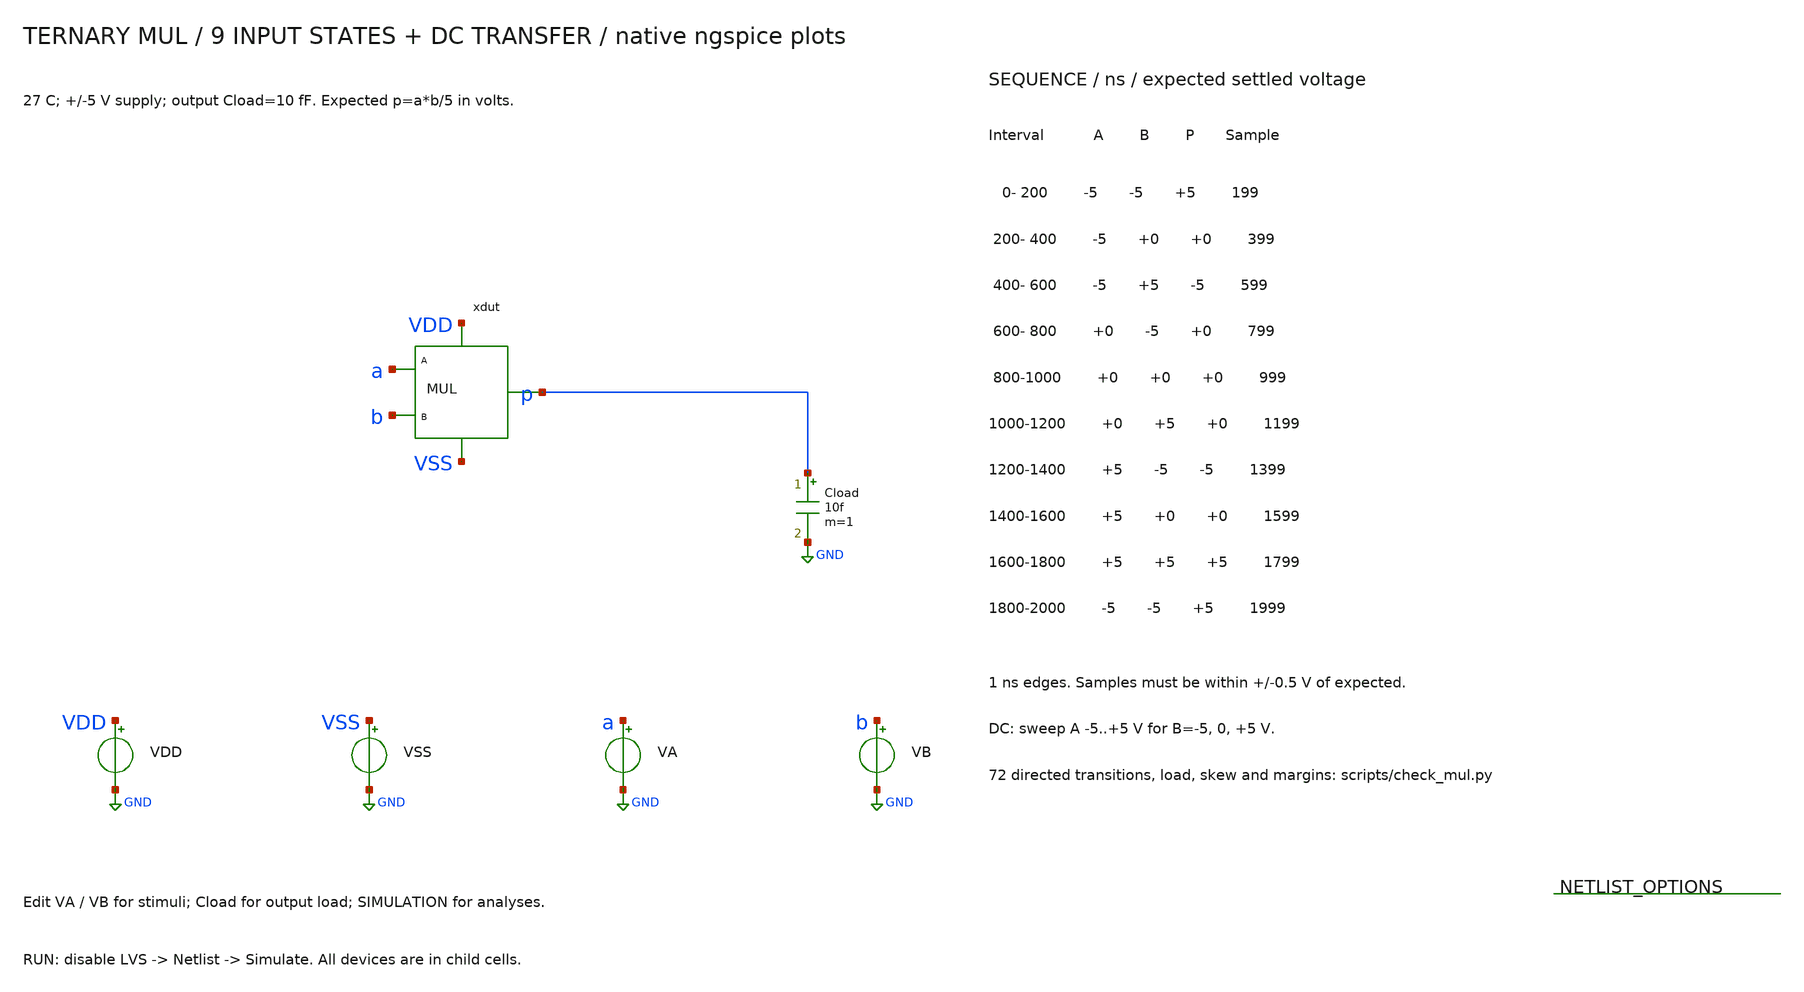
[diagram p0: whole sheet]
** sch_path: mul_tb.sch
**.subckt mul_tb
xdut a b p VDD VSS mul
Cload p GND 10f m=1
VDD VDD GND 5
VSS VSS GND -5
VA a GND PWL(0 -5 200n -5 201n -5 400n -5 401n -5 600n -5 601n 0 800n 0 801n 0 1000n 0 1001n 0 1200n
+ 0 1201n 5 1400n 5 1401n 5 1600n 5 1601n 5 1800n 5 1801n -5 2000n -5)
VB b GND PWL(0 -5 200n -5 201n 0 400n 0 401n 5 600n 5 601n -5 800n -5 801n 0 1000n 0 1001n 5 1200n 5
+ 1201n -5 1400n -5 1401n 0 1600n 0 1601n 5 1800n 5 1801n -5 2000n -5)
**** begin user architecture code
 .include $::LIB/ip62_models

.temp 27
.options rshunt=1e12
.nodeset v(p)=5 v(xdut.t1)=5 v(xdut.t2)=5 v(xdut.t3)=-5
.control
save all
set wr_singlescale
set wr_vecnames
setplot const
let failures=0
alter VB dc=-5
dc VA -5 5 0.03125
meas dc dc_0_0 find v(p) at=-5
if abs(dc_0_0-(5.0)) > 0.5
let const.failures=const.failures+1
echo FAIL: dc_0_0 expected 5.0 V
end
meas dc dc_0_1 find v(p) at=0
if abs(dc_0_1-(0.0)) > 0.5
let const.failures=const.failures+1
echo FAIL: dc_0_1 expected 0.0 V
end
meas dc dc_0_2 find v(p) at=5
if abs(dc_0_2-(-5.0)) > 0.5
let const.failures=const.failures+1
echo FAIL: dc_0_2 expected -5.0 V
end
plot v(a) v(p) ylimit -5.5 5.5 title 'MUL DC: B=-5 V'
wrdata mul_dc_0.txt v(a) v(p) v(xdut.t1) v(xdut.t2) v(xdut.t3)
alter VB dc=0
dc VA -5 5 0.03125
meas dc dc_1_0 find v(p) at=-5
if abs(dc_1_0-(0.0)) > 0.5
let const.failures=const.failures+1
echo FAIL: dc_1_0 expected 0.0 V
end
meas dc dc_1_1 find v(p) at=0
if abs(dc_1_1-(0.0)) > 0.5
let const.failures=const.failures+1
echo FAIL: dc_1_1 expected 0.0 V
end
meas dc dc_1_2 find v(p) at=5
if abs(dc_1_2-(0.0)) > 0.5
let const.failures=const.failures+1
echo FAIL: dc_1_2 expected 0.0 V
end
plot v(a) v(p) ylimit -5.5 5.5 title 'MUL DC: B=0 V'
wrdata mul_dc_1.txt v(a) v(p) v(xdut.t1) v(xdut.t2) v(xdut.t3)
alter VB dc=5
dc VA -5 5 0.03125
meas dc dc_2_0 find v(p) at=-5
if abs(dc_2_0-(-5.0)) > 0.5
let const.failures=const.failures+1
echo FAIL: dc_2_0 expected -5.0 V
end
meas dc dc_2_1 find v(p) at=0
if abs(dc_2_1-(0.0)) > 0.5
let const.failures=const.failures+1
echo FAIL: dc_2_1 expected 0.0 V
end
meas dc dc_2_2 find v(p) at=5
if abs(dc_2_2-(5.0)) > 0.5
let const.failures=const.failures+1
echo FAIL: dc_2_2 expected 5.0 V
end
plot v(a) v(p) ylimit -5.5 5.5 title 'MUL DC: B=5 V'
wrdata mul_dc_2.txt v(a) v(p) v(xdut.t1) v(xdut.t2) v(xdut.t3)
reset
save all
tran 0.2n 2000n 0 0.5n
meas tran p_0 find v(p) at=199n
if abs(p_0-(5.0)) > 0.5
let const.failures=const.failures+1
echo FAIL: p_0 expected 5.0 V
end
meas tran p_1 find v(p) at=399n
if abs(p_1-(0.0)) > 0.5
let const.failures=const.failures+1
echo FAIL: p_1 expected 0.0 V
end
meas tran p_2 find v(p) at=599n
if abs(p_2-(-5.0)) > 0.5
let const.failures=const.failures+1
echo FAIL: p_2 expected -5.0 V
end
meas tran p_3 find v(p) at=799n
if abs(p_3-(0.0)) > 0.5
let const.failures=const.failures+1
echo FAIL: p_3 expected 0.0 V
end
meas tran p_4 find v(p) at=999n
if abs(p_4-(0.0)) > 0.5
let const.failures=const.failures+1
echo FAIL: p_4 expected 0.0 V
end
meas tran p_5 find v(p) at=1199n
if abs(p_5-(0.0)) > 0.5
let const.failures=const.failures+1
echo FAIL: p_5 expected 0.0 V
end
meas tran p_6 find v(p) at=1399n
if abs(p_6-(-5.0)) > 0.5
let const.failures=const.failures+1
echo FAIL: p_6 expected -5.0 V
end
meas tran p_7 find v(p) at=1599n
if abs(p_7-(0.0)) > 0.5
let const.failures=const.failures+1
echo FAIL: p_7 expected 0.0 V
end
meas tran p_8 find v(p) at=1799n
if abs(p_8-(5.0)) > 0.5
let const.failures=const.failures+1
echo FAIL: p_8 expected 5.0 V
end
meas tran p_9 find v(p) at=1999n
if abs(p_9-(5.0)) > 0.5
let const.failures=const.failures+1
echo FAIL: p_9 expected 5.0 V
end
plot v(a) v(b) v(p) ylimit -5.5 5.5 title 'MUL: all nine input states'
plot v(xdut.t1) v(xdut.t2) v(xdut.t3) title 'MUL internal nodes'
wrdata mul_tran.txt v(a) v(b) v(p) v(xdut.t1) v(xdut.t2) v(xdut.t3)
if const.failures = 0
echo PASS: MUL truth table and transient sequence
else
echo FAIL: MUL truth table and transient sequence
end
print const.failures
.endc

**** end user architecture code
**.ends
.GLOBAL GND
.end
